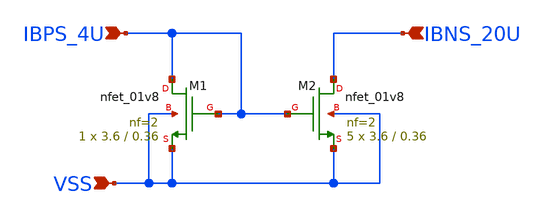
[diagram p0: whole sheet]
** sch_path: design/RPLY_EX0_SKY130NM/RPLY_EX0.sch
**.subckt RPLY_EX0 IBPS_4U VSS IBNS_20U
*.ipin IBPS_4U
*.ipin VSS
*.ipin IBNS_20U
XM1 IBPS_4U IBPS_4U VSS VSS sky130_fd_pr__nfet_01v8 L=0.36 W=3.6 nf=2 ad='int((nf+1)/2) * W/nf * 0.29'
+ as='int((nf+2)/2) * W/nf * 0.29' pd='2*int((nf+1)/2) * (W/nf + 0.29)' ps='2*int((nf+2)/2) * (W/nf + 0.29)'
+ nrd='0.29 / W' nrs='0.29 / W' sa=0 sb=0 sd=0 mult=1 m=1
XM2 IBNS_20U IBPS_4U VSS VSS sky130_fd_pr__nfet_01v8 L=0.36 W=3.6 nf=2 ad='int((nf+1)/2) * W/nf * 0.29'
+ as='int((nf+2)/2) * W/nf * 0.29' pd='2*int((nf+1)/2) * (W/nf + 0.29)' ps='2*int((nf+2)/2) * (W/nf + 0.29)'
+ nrd='0.29 / W' nrs='0.29 / W' sa=0 sb=0 sd=0 mult=5 m=5
**.ends
.end
